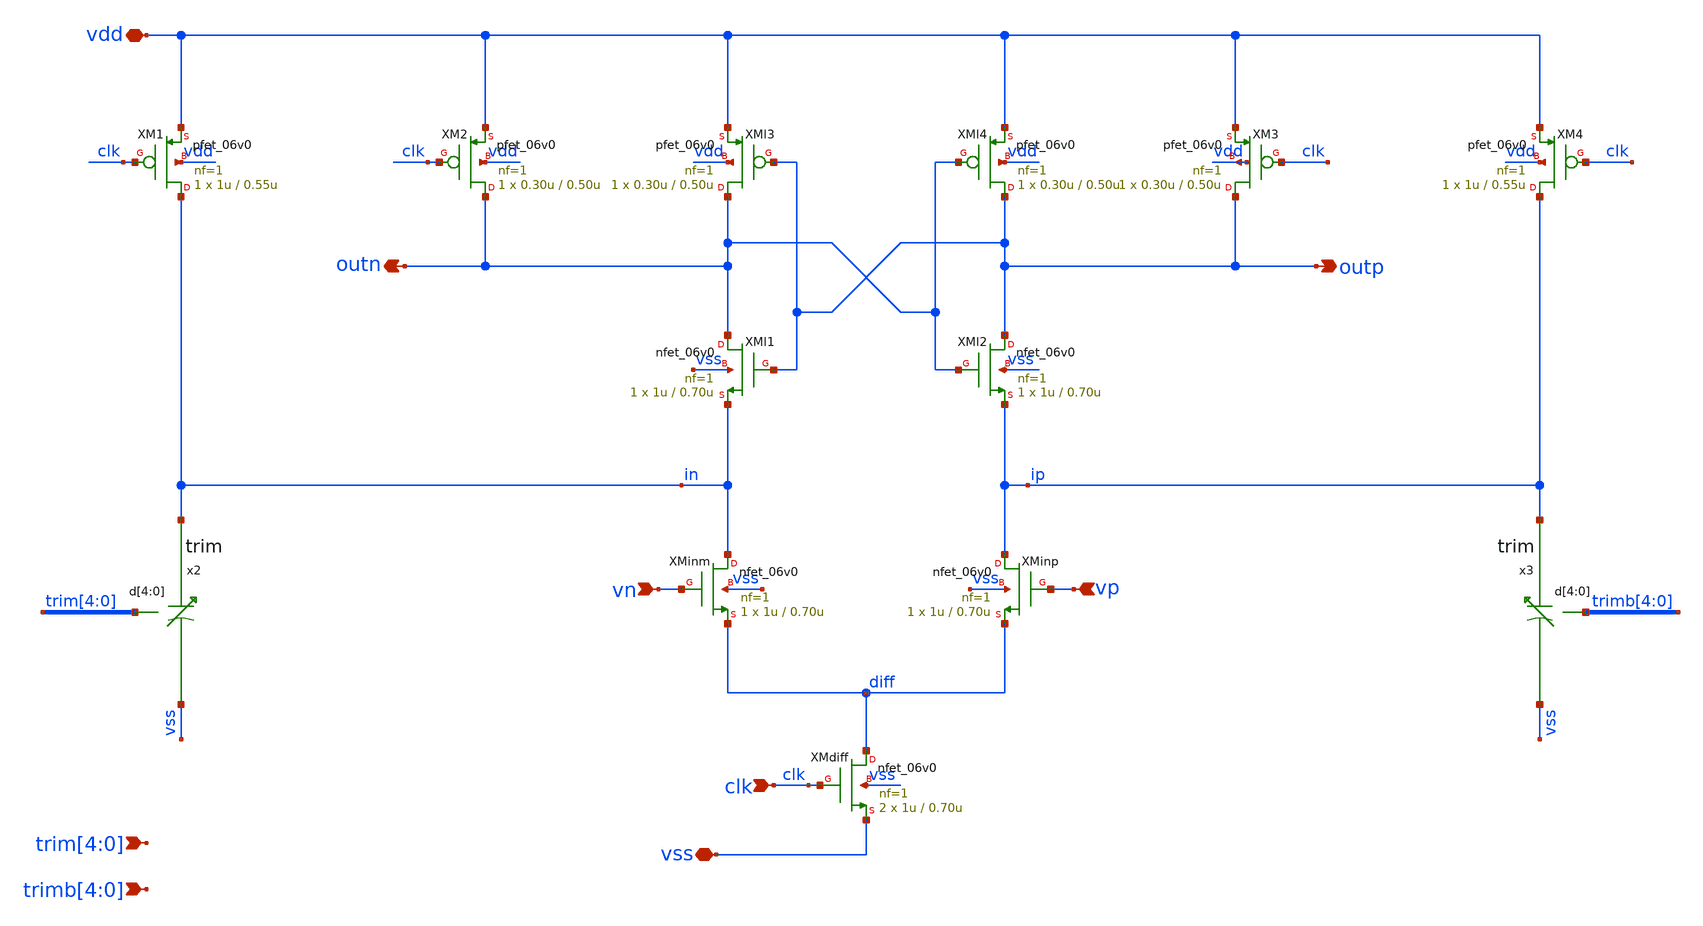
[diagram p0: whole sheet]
** sch_path: xschem/sar_10b/comparator/comparator.sch
**.subckt comparator vn vp clk vdd vss outp outn trim[4],trim[3],trim[2],trim[1],trim[0]
*+ trimb[4],trimb[3],trimb[2],trimb[1],trimb[0]
*.ipin vn
*.ipin vp
*.ipin clk
*.iopin vdd
*.iopin vss
*.opin outp
*.opin outn
*.ipin trim[4],trim[3],trim[2],trim[1],trim[0]
*.ipin trimb[4],trimb[3],trimb[2],trimb[1],trimb[0]
x2 in trim[4] trim[3] trim[2] trim[1] trim[0] vss trim
x3 ip trimb[4] trimb[3] trimb[2] trimb[1] trimb[0] vss trim
XMdiff diff clk vss vss nfet_06v0 L=0.70u W=1u nf=1 ad='int((nf+1)/2) * W/nf * 0.18u' as='int((nf+2)/2) * W/nf * 0.18u'
+ pd='2*int((nf+1)/2) * (W/nf + 0.18u)' ps='2*int((nf+2)/2) * (W/nf + 0.18u)' nrd='0.18u / W' nrs='0.18u / W'
+ sa=0 sb=0 sd=0 m=2
XMinm in vn diff vss nfet_06v0 L=0.70u W=1u nf=1 ad='int((nf+1)/2) * W/nf * 0.18u' as='int((nf+2)/2) * W/nf * 0.18u'
+ pd='2*int((nf+1)/2) * (W/nf + 0.18u)' ps='2*int((nf+2)/2) * (W/nf + 0.18u)' nrd='0.18u / W' nrs='0.18u / W'
+ sa=0 sb=0 sd=0 m=1
XMinp ip vp diff vss nfet_06v0 L=0.70u W=1u nf=1 ad='int((nf+1)/2) * W/nf * 0.18u' as='int((nf+2)/2) * W/nf * 0.18u'
+ pd='2*int((nf+1)/2) * (W/nf + 0.18u)' ps='2*int((nf+2)/2) * (W/nf + 0.18u)' nrd='0.18u / W' nrs='0.18u / W'
+ sa=0 sb=0 sd=0 m=1
XMl1 outn outp in vss nfet_06v0 L=0.70u W=1u nf=1 ad='int((nf+1)/2) * W/nf * 0.18u' as='int((nf+2)/2) * W/nf * 0.18u'
+ pd='2*int((nf+1)/2) * (W/nf + 0.18u)' ps='2*int((nf+2)/2) * (W/nf + 0.18u)' nrd='0.18u / W' nrs='0.18u / W'
+ sa=0 sb=0 sd=0 m=1
XMl2 outp outn ip vss nfet_06v0 L=0.70u W=1u nf=1 ad='int((nf+1)/2) * W/nf * 0.18u' as='int((nf+2)/2) * W/nf * 0.18u'
+ pd='2*int((nf+1)/2) * (W/nf + 0.18u)' ps='2*int((nf+2)/2) * (W/nf + 0.18u)' nrd='0.18u / W' nrs='0.18u / W'
+ sa=0 sb=0 sd=0 m=1
XM1 in clk vdd vdd pfet_06v0 L=0.55u W=1u nf=1 ad='int((nf+1)/2) * W/nf * 0.18u' as='int((nf+2)/2) * W/nf * 0.18u'
+ pd='2*int((nf+1)/2) * (W/nf + 0.18u)' ps='2*int((nf+2)/2) * (W/nf + 0.18u)' nrd='0.18u / W' nrs='0.18u / W'
+ sa=0 sb=0 sd=0 m=1
XM2 outn clk vdd vdd pfet_06v0 L=0.50u W=0.30u nf=1 ad='int((nf+1)/2) * W/nf * 0.18u' as='int((nf+2)/2) * W/nf * 0.18u'
+ pd='2*int((nf+1)/2) * (W/nf + 0.18u)' ps='2*int((nf+2)/2) * (W/nf + 0.18u)' nrd='0.18u / W' nrs='0.18u / W'
+ sa=0 sb=0 sd=0 m=1
XMl3 outn outp vdd vdd pfet_06v0 L=0.50u W=0.30u nf=1 ad='int((nf+1)/2) * W/nf * 0.18u' as='int((nf+2)/2) * W/nf * 0.18u'
+ pd='2*int((nf+1)/2) * (W/nf + 0.18u)' ps='2*int((nf+2)/2) * (W/nf + 0.18u)' nrd='0.18u / W' nrs='0.18u / W'
+ sa=0 sb=0 sd=0 m=1
XM4 ip clk vdd vdd pfet_06v0 L=0.55u W=1u nf=1 ad='int((nf+1)/2) * W/nf * 0.18u' as='int((nf+2)/2) * W/nf * 0.18u'
+ pd='2*int((nf+1)/2) * (W/nf + 0.18u)' ps='2*int((nf+2)/2) * (W/nf + 0.18u)' nrd='0.18u / W' nrs='0.18u / W'
+ sa=0 sb=0 sd=0 m=1
XM3 outp clk vdd vdd pfet_06v0 L=0.50u W=0.30u nf=1 ad='int((nf+1)/2) * W/nf * 0.18u' as='int((nf+2)/2) * W/nf * 0.18u'
+ pd='2*int((nf+1)/2) * (W/nf + 0.18u)' ps='2*int((nf+2)/2) * (W/nf + 0.18u)' nrd='0.18u / W' nrs='0.18u / W'
+ sa=0 sb=0 sd=0 m=1
XMl4 outp outn vdd vdd pfet_06v0 L=0.50u W=0.30u nf=1 ad='int((nf+1)/2) * W/nf * 0.18u' as='int((nf+2)/2) * W/nf * 0.18u'
+ pd='2*int((nf+1)/2) * (W/nf + 0.18u)' ps='2*int((nf+2)/2) * (W/nf + 0.18u)' nrd='0.18u / W' nrs='0.18u / W'
+ sa=0 sb=0 sd=0 m=1
**.ends

* expanding   symbol:  sar_10b/comparator/trim.sym # of pins=3
** sym_path: sar_10b/comparator/trim.sym
** sch_path: sar_10b/comparator/trim.sch
.subckt trim drain d[4] d[3] d[2] d[1] d[0] vss
*.iopin vss
*.ipin d[4],d[3],d[2],d[1],d[0]
*.opin drain
x4[7] drain n4 trimcap
x4[6] drain n4 trimcap
x4[5] drain n4 trimcap
x4[4] drain n4 trimcap
x4[3] drain n4 trimcap
x4[2] drain n4 trimcap
x4[1] drain n4 trimcap
x4[0] drain n4 trimcap
x3[3] drain n3 trimcap
x3[2] drain n3 trimcap
x3[1] drain n3 trimcap
x3[0] drain n3 trimcap
x2[1] drain n2 trimcap
x2[0] drain n2 trimcap
x1 drain n1 trimcap
x0 drain n0 trimcap
XM0 n0 d[0] vss vss nfet_06v0 L=0.70u W=1u nf=1 ad='int((nf+1)/2) * W/nf * 0.18u' as='int((nf+2)/2) * W/nf * 0.18u'
+ pd='2*int((nf+1)/2) * (W/nf + 0.18u)' ps='2*int((nf+2)/2) * (W/nf + 0.18u)' nrd='0.18u / W' nrs='0.18u / W'
+ sa=0 sb=0 sd=0 m=1
XM1 n1 d[1] vss vss nfet_06v0 L=0.70u W=1u nf=1 ad='int((nf+1)/2) * W/nf * 0.18u' as='int((nf+2)/2) * W/nf * 0.18u'
+ pd='2*int((nf+1)/2) * (W/nf + 0.18u)' ps='2*int((nf+2)/2) * (W/nf + 0.18u)' nrd='0.18u / W' nrs='0.18u / W'
+ sa=0 sb=0 sd=0 m=1
XM2 n2 d[2] vss vss nfet_06v0 L=0.70u W=1u nf=1 ad='int((nf+1)/2) * W/nf * 0.18u' as='int((nf+2)/2) * W/nf * 0.18u'
+ pd='2*int((nf+1)/2) * (W/nf + 0.18u)' ps='2*int((nf+2)/2) * (W/nf + 0.18u)' nrd='0.18u / W' nrs='0.18u / W'
+ sa=0 sb=0 sd=0 m=2
XM3 n3 d[3] vss vss nfet_06v0 L=0.70u W=1u nf=1 ad='int((nf+1)/2) * W/nf * 0.18u' as='int((nf+2)/2) * W/nf * 0.18u'
+ pd='2*int((nf+1)/2) * (W/nf + 0.18u)' ps='2*int((nf+2)/2) * (W/nf + 0.18u)' nrd='0.18u / W' nrs='0.18u / W'
+ sa=0 sb=0 sd=0 m=4
XM4 n4 d[4] vss vss nfet_06v0 L=0.70u W=1u nf=1 ad='int((nf+1)/2) * W/nf * 0.18u' as='int((nf+2)/2) * W/nf * 0.18u'
+ pd='2*int((nf+1)/2) * (W/nf + 0.18u)' ps='2*int((nf+2)/2) * (W/nf + 0.18u)' nrd='0.18u / W' nrs='0.18u / W'
+ sa=0 sb=0 sd=0 m=8
.ends


* expanding   symbol:  sar_10b/comparator/trimcap.sym # of pins=2
** sym_path: sar_10b/comparator/trimcap.sym
** sch_path: sar_10b/comparator/trimcap.sch
.subckt trimcap cp cn
*.iopin cp
*.iopin cn
c0 cp cn 1f m=1
.ends

.end
